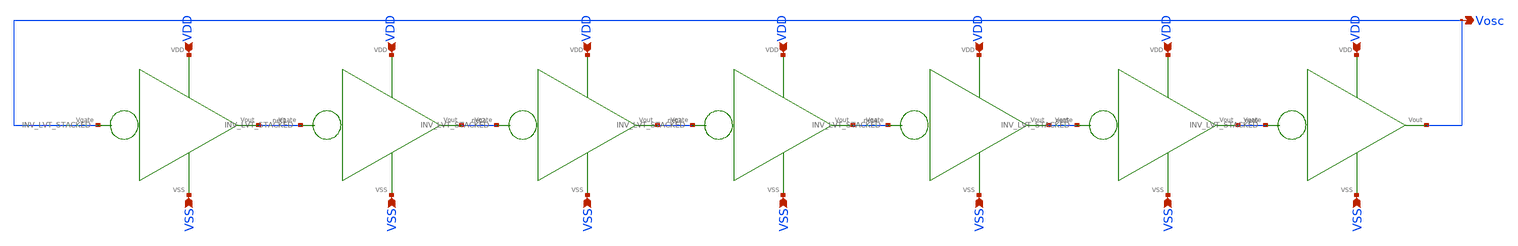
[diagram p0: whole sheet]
** sch_path: design/THESIS_EXP_RO_INVERTER_SKY130A/RO_LVT_STACKED.sch
**.subckt RO_LVT_STACKED VSS VSS VSS VSS VSS VSS VSS VDD VDD VDD VDD VDD VDD VDD Vosc
*.ipin VSS
*.ipin VSS
*.ipin VSS
*.ipin VSS
*.ipin VSS
*.ipin VSS
*.ipin VSS
*.ipin VDD
*.ipin VDD
*.ipin VDD
*.ipin VDD
*.ipin VDD
*.ipin VDD
*.ipin VDD
*.opin Vosc
X1 Vosc net1 VSS VDD INV_LVT_STACKED
X2 net1 net2 VSS VDD INV_LVT_STACKED
X3 net2 net3 VSS VDD INV_LVT_STACKED
X4 net3 net4 VSS VDD INV_LVT_STACKED
X5 net4 net5 VSS VDD INV_LVT_STACKED
X6 net5 net6 VSS VDD INV_LVT_STACKED
X7 net6 Vosc VSS VDD INV_LVT_STACKED
**.ends
.end
